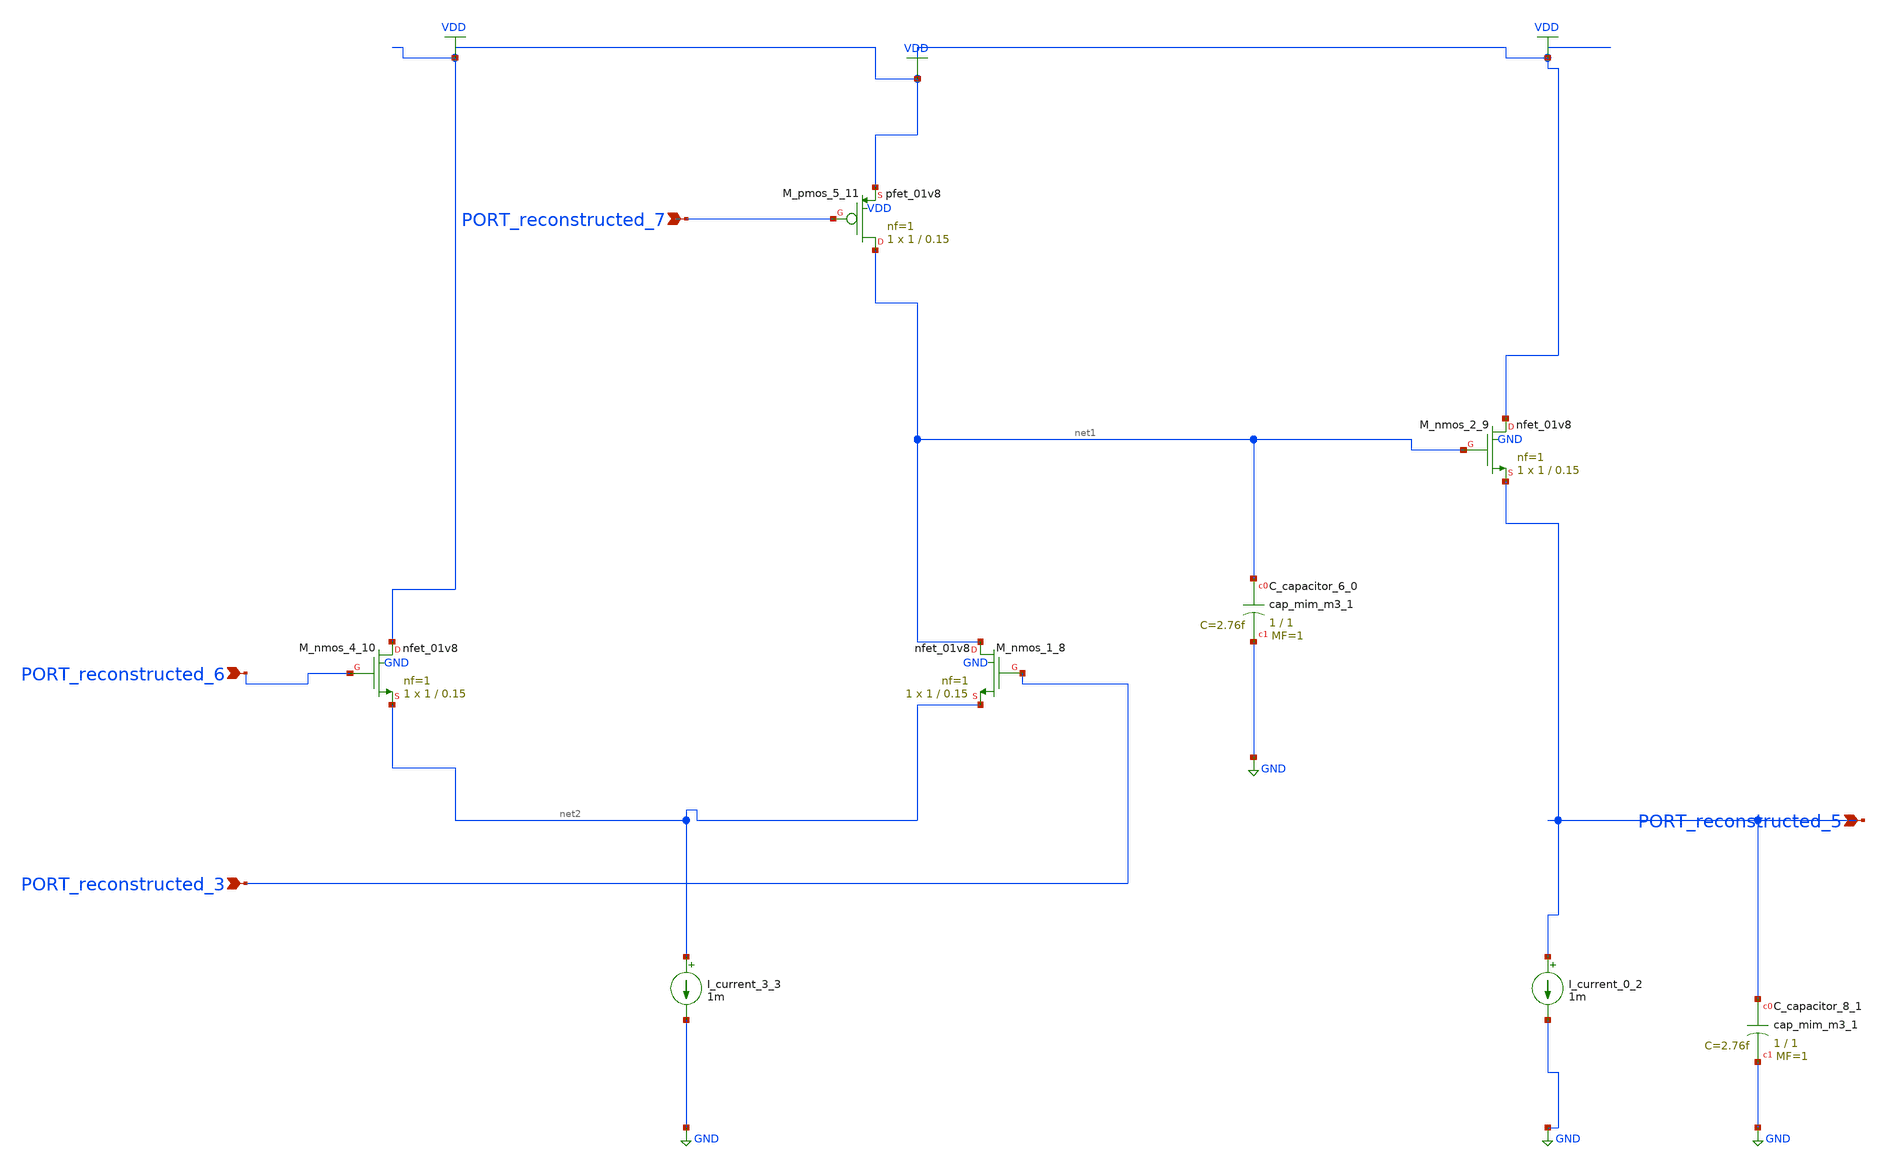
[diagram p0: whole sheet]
** sch_path: schematics/AMSNet/741.sch
**.subckt 741 PORT_reconstructed_5 PORT_reconstructed_3 PORT_reconstructed_7 PORT_reconstructed_6
*.ipin PORT_reconstructed_5
*.ipin PORT_reconstructed_3
*.ipin PORT_reconstructed_7
*.ipin PORT_reconstructed_6
XC_capacitor_6_0 net1 GND sky130_fd_pr__cap_mim_m3_1 W=1 L=1 MF=1 m=1
XC_capacitor_8_1 PORT_reconstructed_5 GND sky130_fd_pr__cap_mim_m3_1 W=1 L=1 MF=1 m=1
I_current_0_2 PORT_reconstructed_5 GND 1m
I_current_3_3 net2 GND 1m
XM_nmos_1_8 net1 PORT_reconstructed_3 net2 GND sky130_fd_pr__nfet_01v8 L=0.15 W=1 nf=1 ad='int((1 + 1)/2) * 1 / 1 * 0.29'
+ as='int((1 + 2)/2) * 1 / 1 * 0.29' pd='2*int((1 + 1)/2) * (1 / 1 + 0.29)' ps='2*int((1 + 2)/2) * (1 / 1 + 0.29)'
+ nrd='0.29 / 1 ' nrs='0.29 / 1 ' sa=0 sb=0 sd=0 mult=1 m=1
XM_nmos_2_9 VDD net1 PORT_reconstructed_5 GND sky130_fd_pr__nfet_01v8 L=0.15 W=1 nf=1 ad='int((1 + 1)/2) * 1 / 1 * 0.29'
+ as='int((1 + 2)/2) * 1 / 1 * 0.29' pd='2*int((1 + 1)/2) * (1 / 1 + 0.29)' ps='2*int((1 + 2)/2) * (1 / 1 + 0.29)'
+ nrd='0.29 / 1 ' nrs='0.29 / 1 ' sa=0 sb=0 sd=0 mult=1 m=1
XM_nmos_4_10 VDD PORT_reconstructed_6 net2 GND sky130_fd_pr__nfet_01v8 L=0.15 W=1 nf=1 ad='int((1 + 1)/2) * 1 / 1 * 0.29'
+ as='int((1 + 2)/2) * 1 / 1 * 0.29' pd='2*int((1 + 1)/2) * (1 / 1 + 0.29)' ps='2*int((1 + 2)/2) * (1 / 1 + 0.29)'
+ nrd='0.29 / 1 ' nrs='0.29 / 1 ' sa=0 sb=0 sd=0 mult=1 m=1
XM_pmos_5_11 net1 PORT_reconstructed_7 VDD VDD sky130_fd_pr__pfet_01v8 L=0.15 W=1 nf=1 ad='int((1 + 1)/2) * 1 / 1 * 0.29'
+ as='int((1 + 2)/2) * 1 / 1 * 0.29' pd='2*int((1 + 1)/2) * (1 / 1 + 0.29)' ps='2*int((1 + 2)/2) * (1 / 1 + 0.29)'
+ nrd='0.29 / 1 ' nrs='0.29 / 1 ' sa=0 sb=0 sd=0 mult=1 m=1
**.ends
.GLOBAL GND
.GLOBAL VDD
.end
